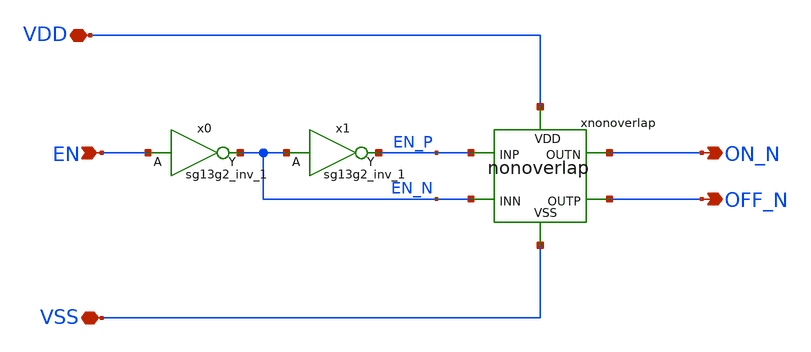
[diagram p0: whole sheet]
** sch_path: xschem/switch_logic_nonoverlap.sch
**.subckt switch_logic_nonoverlap VSS VDD EN ON_N OFF_N
*.iopin VSS
*.iopin VDD
*.ipin EN
*.opin ON_N
*.opin OFF_N
x0 EN_N EN VDD VSS sg13g2_inv_1
x1 EN_P EN_N VDD VSS sg13g2_inv_1
xnonoverlap VDD VSS EN_P EN_N ON_N OFF_N nonoverlap
**.ends

* expanding   symbol:  sg13g2_stdcells/sg13g2_inv_1.sym # of pins=2
** sym_path: sg13g2_stdcells/sg13g2_inv_1.sym
** sch_path: sg13g2_stdcells/sg13g2_inv_1.sch
.subckt sg13g2_inv_1 Y A VDD VSS
*.opin Y
*.ipin A
*.iopin VDD
*.iopin VSS
XM1 Y A VSS VSS sg13_lv_nmos w=740.00n l=130.00n ng=1 m=1 mm_ok=1
XM2 Y A VDD VDD sg13_lv_pmos w=1.12u l=130.00n ng=1 m=1 mm_ok=1
.ends


* expanding   symbol:  nonoverlap.sym # of pins=6
** sym_path: xschem/nonoverlap.sym
** sch_path: xschem/nonoverlap.sch
.subckt nonoverlap VDD VSS INP INN OUTN OUTP
*.iopin VSS
*.iopin VDD
*.ipin INP
*.ipin INN
*.opin OUTP
*.opin OUTN
XM1 OUTN INP VDD VDD sg13_lv_pmos w=0.3u l=0.13u ng=1 m=1 mm_ok=1
XM2 OUTP INN VDD VDD sg13_lv_pmos w=0.3u l=0.13u ng=1 m=1 mm_ok=1
XM3 OUTN OUTP VSS VSS sg13_lv_nmos w=0.15u l=0.52u ng=1 m=1 mm_ok=1
XM4 OUTP OUTN VSS VSS sg13_lv_nmos w=0.15u l=0.52u ng=1 m=1 mm_ok=1
.ends

.end
